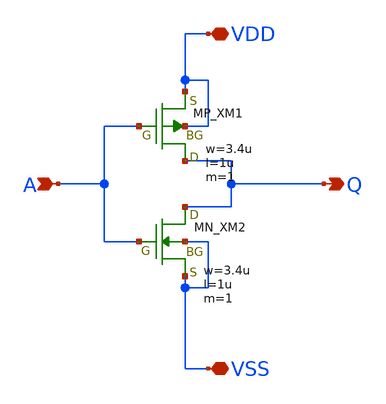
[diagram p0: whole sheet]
** sch_path: schematic/20250924_OSS_Workshop/Qdai/inverter_MUX_01/inv_fujiimakoto.sch
**.subckt inv_fujiimakoto VDD A VSS Q
*.iopin VDD
*.ipin A
*.iopin VSS
*.opin Q
XM1 Q A VDD VDD PMOS w=3.4u l=1u as=0 ad=0 ps=0 pd=0 nrd=0 nrs=0 m=1
XM2 Q A VSS VSS NMOS w=3.4u l=1u as=0 ad=0 ps=0 pd=0 nrd=0 nrs=0 m=1
**.ends
.end
